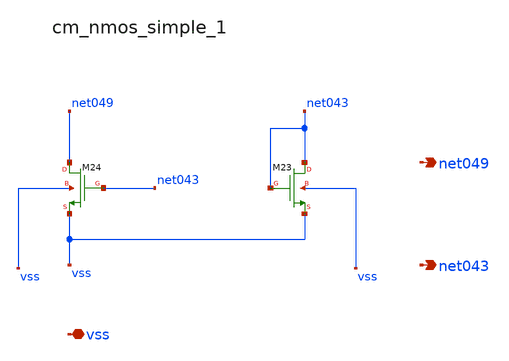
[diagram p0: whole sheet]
** sch_path: analog-db/raw/amp_007_leung_dfcfc2/hier/blocks/cm_nmos_simple_1.sch
**.subckt cm_nmos_simple_1 vss net049 net043
*.iopin vss
*.opin net049
*.opin net043
XM23 net043 net043 vss vss sg13_lv_nmos w=x_dut_xm23_w l=x_dut_xm23_l ng=1 m=x_dut_xm23_m
XM24 net049 net043 vss vss sg13_lv_nmos w=x_dut_xm24_w l=x_dut_xm24_l ng=1 m=x_dut_xm24_m
**.ends
.end
